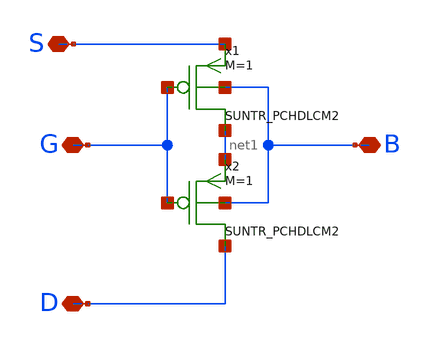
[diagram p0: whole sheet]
** sch_path: design/RPLY_BIAS_SKY130NM/RPLYBS_PMOS.sch
**.subckt RPLYBS_PMOS G D S B
*.iopin G
*.iopin D
*.iopin S
*.iopin B
x1 net1 G S B SUNTR_PCHDLCM2 xoffset=0 yoffset=0 angle=0 M=1
x2 D G net1 B SUNTR_PCHDLCM2 xoffset=0 yoffset=0 angle=0 M=1
**.ends
.end
